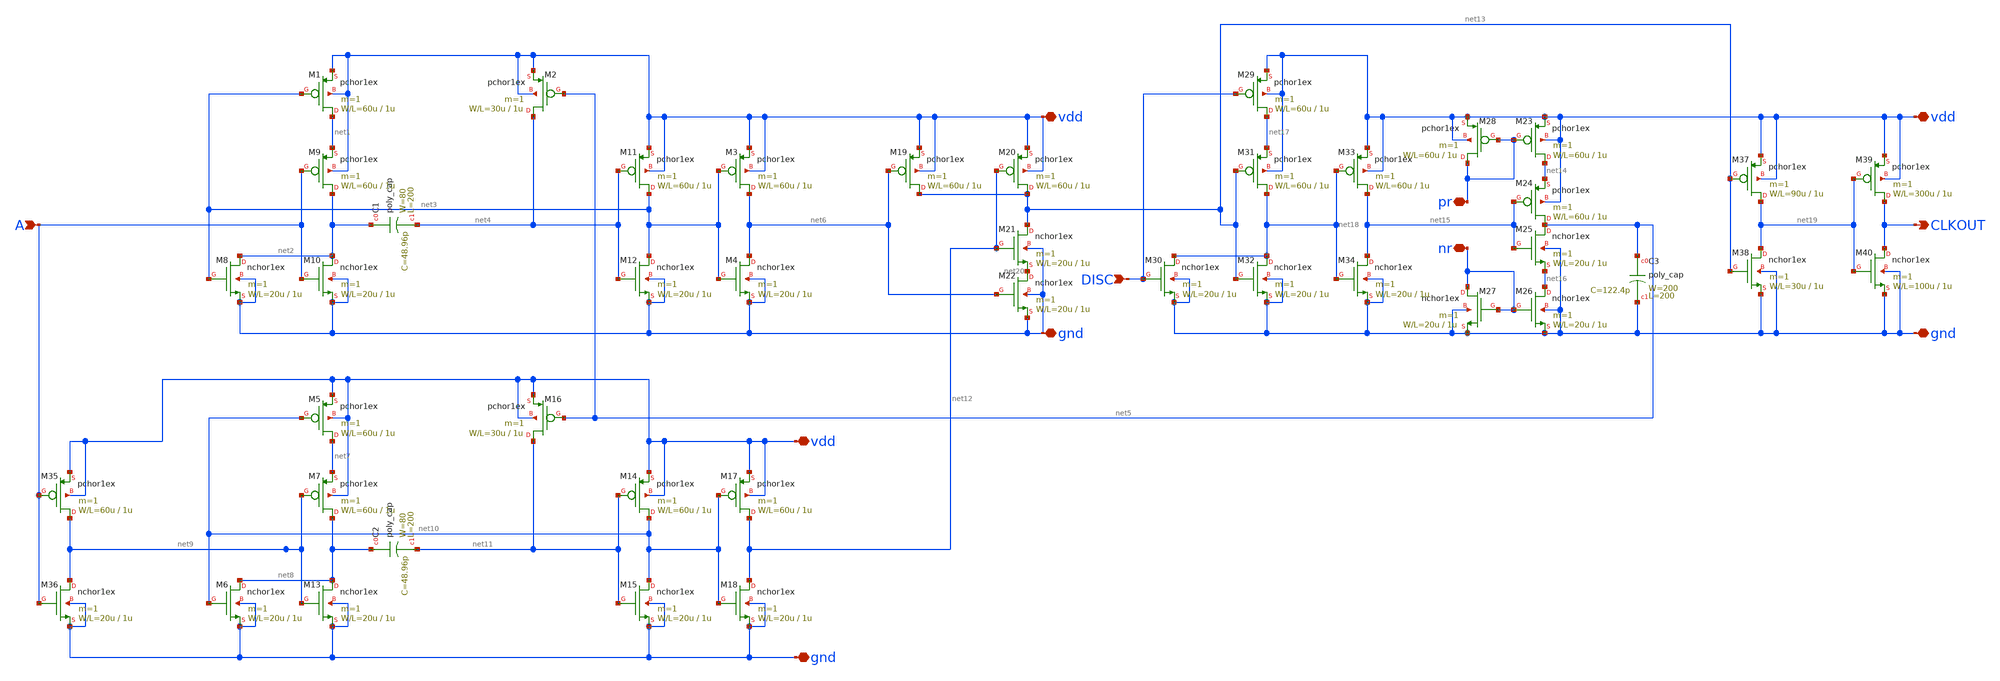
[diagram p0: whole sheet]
** sch_path: member_project/3zki/clkdb.sch
**.subckt clkdb vdd gnd A vdd gnd pr nr vdd gnd DISC CLKOUT
*.iopin vdd
*.iopin gnd
*.ipin A
*.iopin vdd
*.iopin gnd
*.iopin pr
*.iopin nr
*.iopin vdd
*.iopin gnd
*.ipin DISC
*.opin CLKOUT
M1 net1 net3 vdd vdd pchor1ex L=1u W=60u m=1
M8 net2 net3 gnd gnd nchor1ex L=1u W=20u m=1
M9 net2 A net1 vdd pchor1ex L=1u W=60u m=1
M10 net2 A gnd gnd nchor1ex L=1u W=20u m=1
M11 net3 net4 vdd vdd pchor1ex L=1u W=60u m=1
M12 net3 net4 gnd gnd nchor1ex L=1u W=20u m=1
C1 net2 net4 poly_cap W=80 L=200
M2 net4 net5 vdd vdd pchor1ex L=1u W=30u m=1
M3 net6 net3 vdd vdd pchor1ex L=1u W=60u m=1
M4 net6 net3 gnd gnd nchor1ex L=1u W=20u m=1
M5 net7 net10 vdd vdd pchor1ex L=1u W=60u m=1
M6 net8 net10 gnd gnd nchor1ex L=1u W=20u m=1
M7 net8 net9 net7 vdd pchor1ex L=1u W=60u m=1
M13 net8 net9 gnd gnd nchor1ex L=1u W=20u m=1
M14 net10 net11 vdd vdd pchor1ex L=1u W=60u m=1
M15 net10 net11 gnd gnd nchor1ex L=1u W=20u m=1
C2 net8 net11 poly_cap W=80 L=200
M16 net11 net5 vdd vdd pchor1ex L=1u W=30u m=1
M17 net12 net10 vdd vdd pchor1ex L=1u W=60u m=1
M18 net12 net10 gnd gnd nchor1ex L=1u W=20u m=1
M35 net9 A vdd vdd pchor1ex L=1u W=60u m=1
M36 net9 A gnd gnd nchor1ex L=1u W=20u m=1
M19 net13 net6 vdd vdd pchor1ex L=1u W=60u m=1
M20 net13 net12 vdd vdd pchor1ex L=1u W=60u m=1
M21 net13 net12 net20 gnd nchor1ex L=1u W=20u m=1
M22 net20 net6 gnd gnd nchor1ex L=1u W=20u m=1
M23 net14 pr vdd vdd pchor1ex L=1u W=60u m=1
M24 net5 net15 net14 vdd pchor1ex L=1u W=60u m=1
M25 net5 net15 net16 gnd nchor1ex L=1u W=20u m=1
M26 net16 nr gnd gnd nchor1ex L=1u W=20u m=1
M27 nr nr gnd gnd nchor1ex L=1u W=20u m=1
M28 pr pr vdd vdd pchor1ex L=1u W=60u m=1
C3 net5 gnd poly_cap W=200 L=200
M29 net17 DISC vdd vdd pchor1ex L=1u W=60u m=1
M30 net18 DISC gnd gnd nchor1ex L=1u W=20u m=1
M31 net18 net13 net17 vdd pchor1ex L=1u W=60u m=1
M32 net18 net13 gnd gnd nchor1ex L=1u W=20u m=1
M33 net15 net18 vdd vdd pchor1ex L=1u W=60u m=1
M34 net15 net18 gnd gnd nchor1ex L=1u W=20u m=1
M37 net19 net13 vdd vdd pchor1ex L=1u W=90u m=1
M38 net19 net13 gnd gnd nchor1ex L=1u W=30u m=1
M39 CLKOUT net19 vdd vdd pchor1ex L=1u W=300u m=1
M40 CLKOUT net19 gnd gnd nchor1ex L=1u W=100u m=1
**.ends
.end
